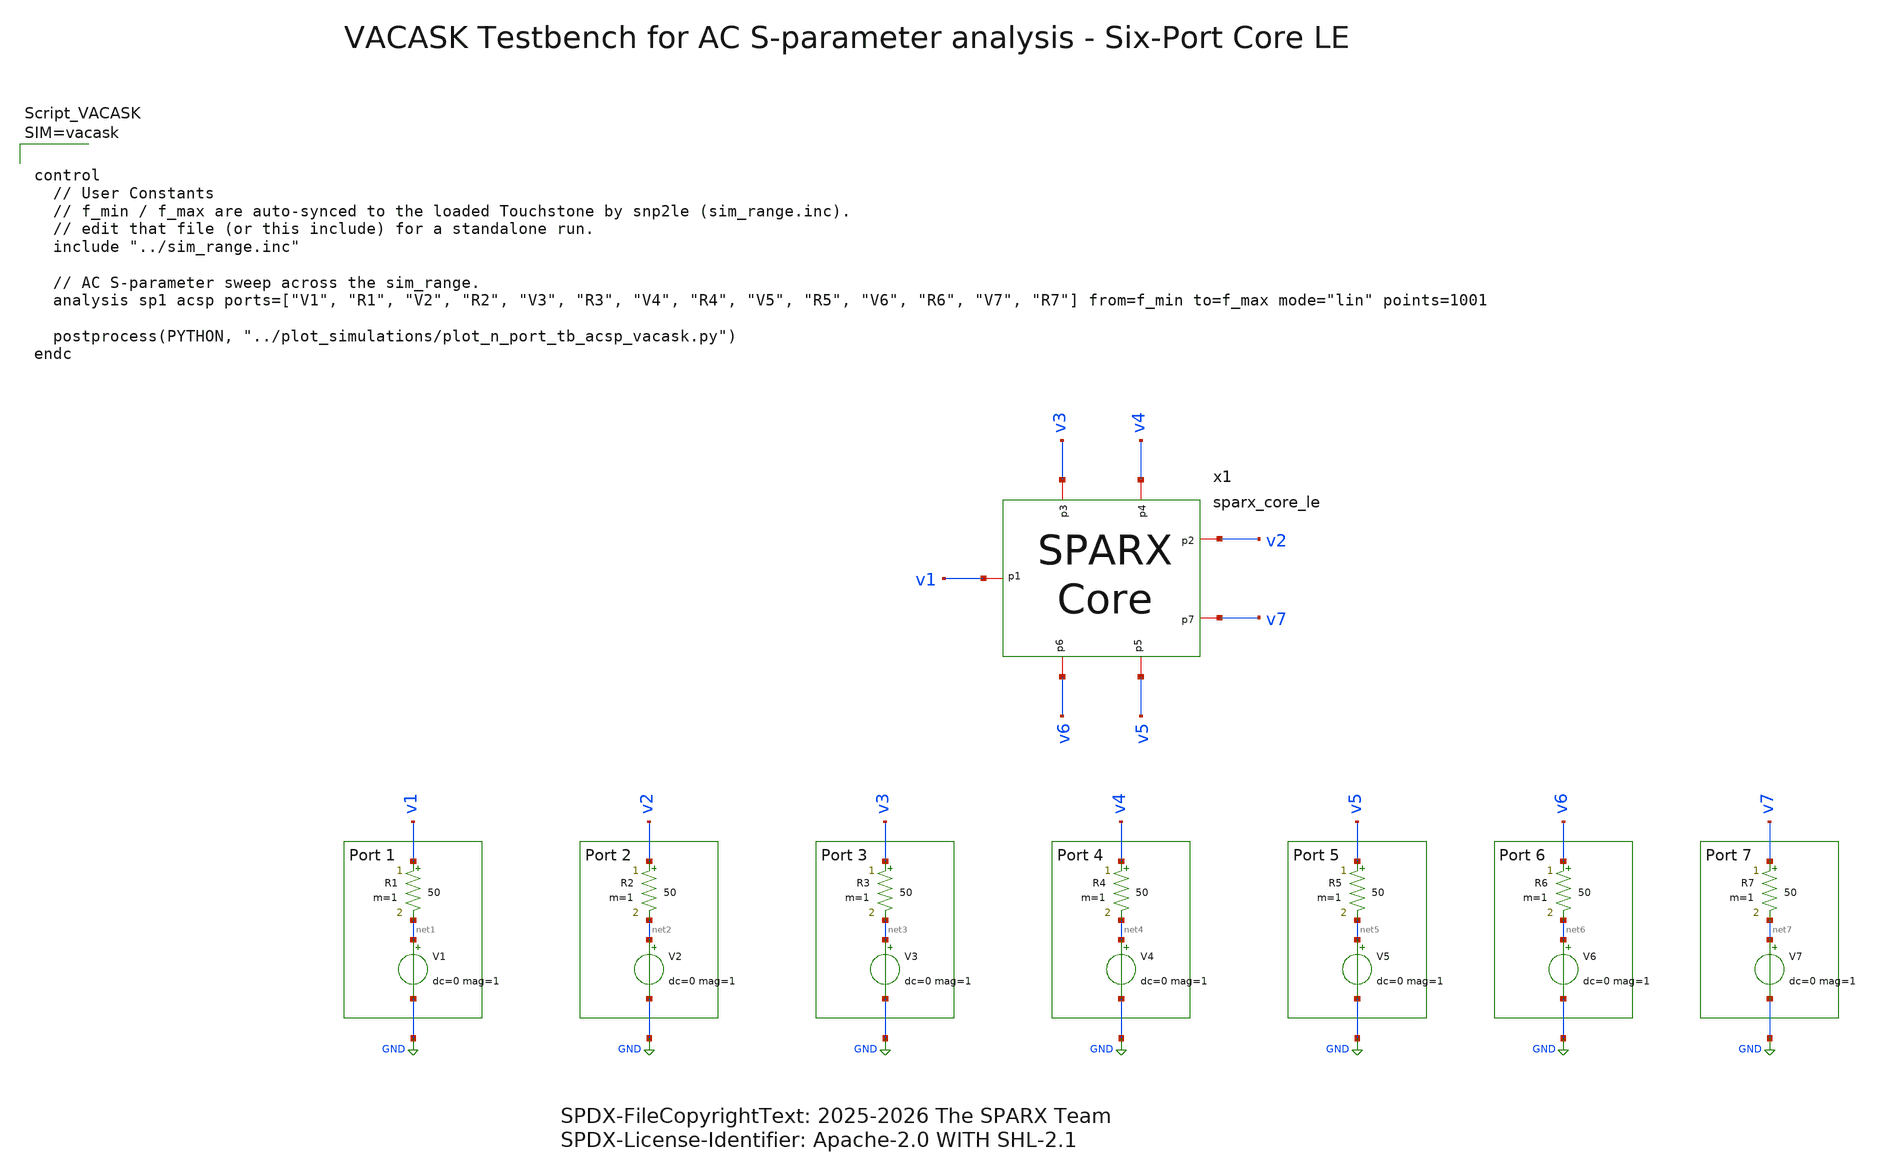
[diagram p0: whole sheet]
** sch_path: testbenches/xschem/sparx_core_le_tb_acsp_vacask.sch
* SPDX-FileCopyrightText: 2025-2026 The SPARX Team
* SPDX-License-Identifier: Apache-2.0 WITH SHL-2.1
**.subckt sparx_core_le_tb_acsp_vacask
R1 v1 net1 50 m=1
V1 net1 GND dc=0 mag=1
R2 v2 net2 50 m=1
V2 net2 GND dc=0 mag=1
R3 v3 net3 50 m=1
V3 net3 GND dc=0 mag=1
R4 v4 net4 50 m=1
V4 net4 GND dc=0 mag=1
R5 v5 net5 50 m=1
V5 net5 GND dc=0 mag=1
R6 v6 net6 50 m=1
V6 net6 GND dc=0 mag=1
R7 v7 net7 50 m=1
V7 net7 GND dc=0 mag=1
x1 v3 v4 v2 v1 v7 v5 v6 sparx_core_le
**** begin user architecture code






**** end user architecture code
**.ends
.GLOBAL GND
.end
